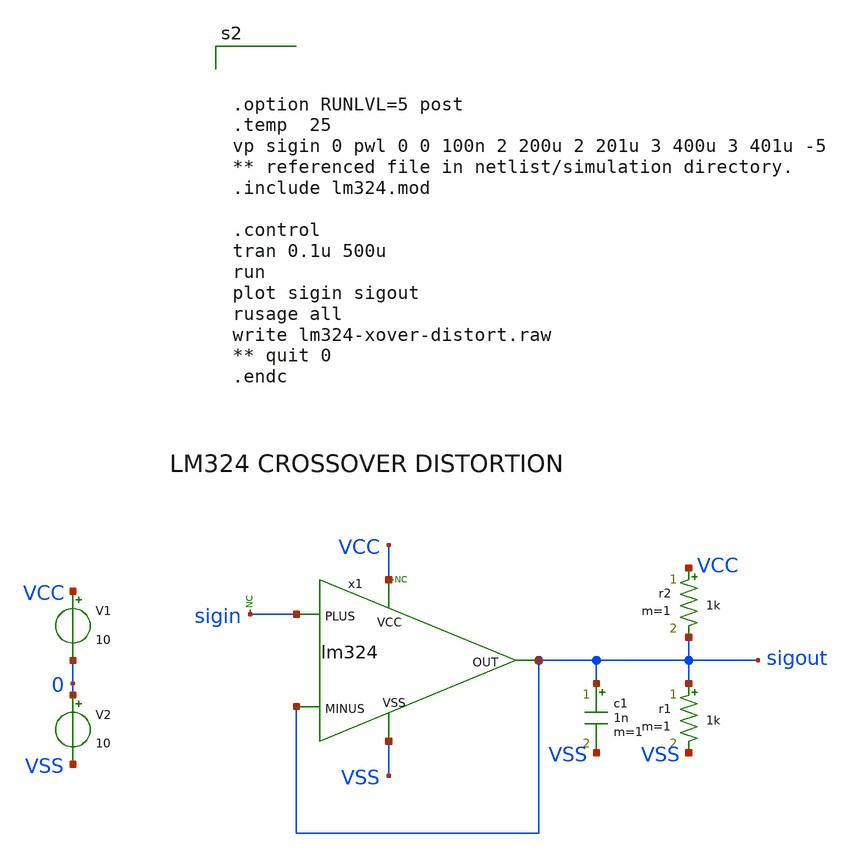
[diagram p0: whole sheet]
** sch_path: lm324-xover-distort.sch
* Copyright (C) 1998-2024 Stefan Frederik Schippers
* This program is free software; you can redistribute it and/or modify
* it under the terms of the GNU General Public License as published by
* the Free Software Foundation; either version 2 of the License, or
* (at your option) any later version.
* This program is distributed in the hope that it will be useful,
* but WITHOUT ANY WARRANTY; without even the implied warranty of
* MERCHANTABILITY or FITNESS FOR A PARTICULAR PURPOSE.  See the
* GNU General Public License for more details.
* You should have received a copy of the GNU General Public License
* along with this program; if not, write to the Free Software
**.subckt lm324-xover-distort
x1 sigin sigout VCC VSS sigout lm324
r1 sigout VSS 1k m=1
c1 sigout VSS 1n m=1
* noconn sigin
* noconn VCC
r2 VCC sigout 1k m=1
V1 VCC 0 10
V2 0 VSS 10
**** begin user architecture code



.option RUNLVL=5 post
.temp  25
vp sigin 0 pwl 0 0 100n 2 200u 2 201u 3 400u 3 401u -5
** referenced file in netlist/simulation directory.
.include lm324.mod

.control
tran 0.1u 500u
run
plot sigin sigout
rusage all
write lm324-xover-distort.raw
** quit 0
.endc


**** end user architecture code
**.ends
.end
